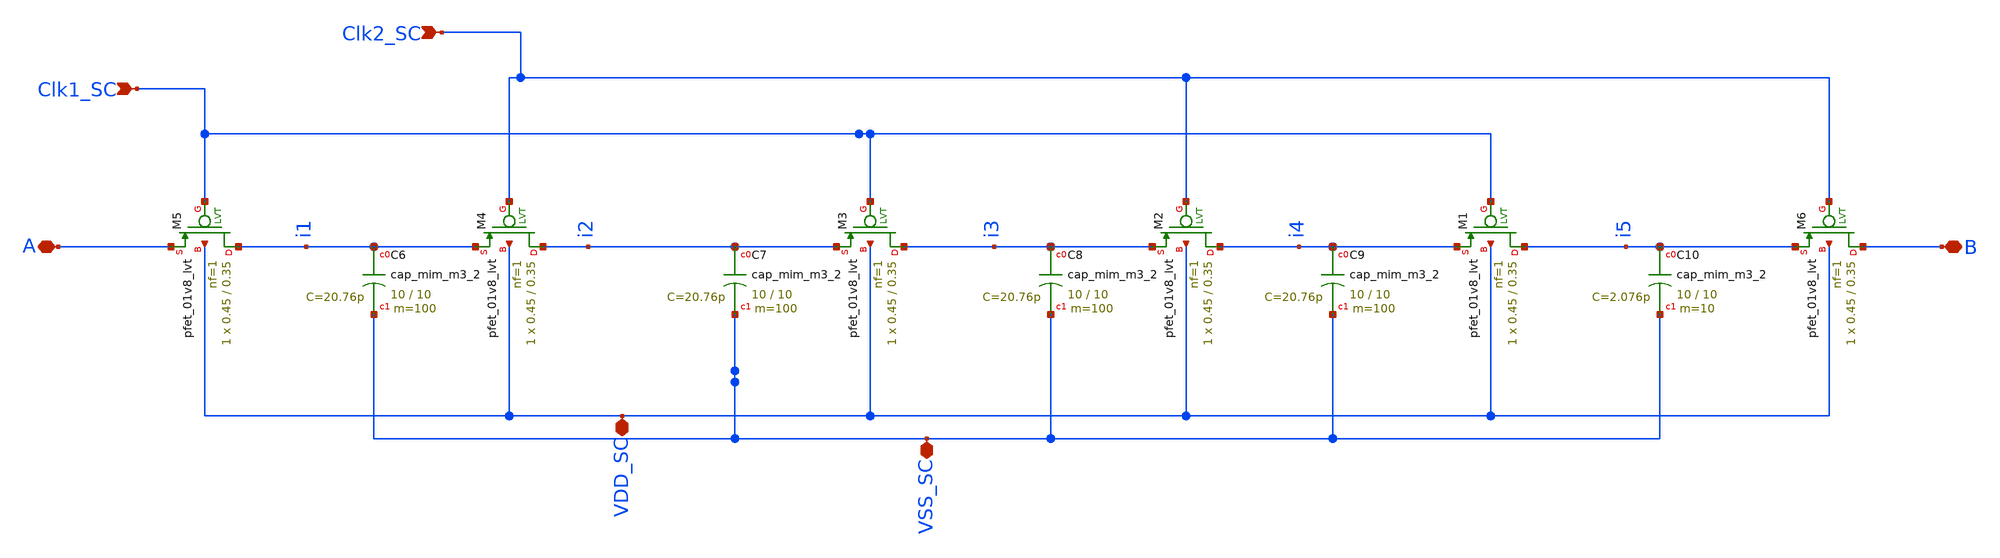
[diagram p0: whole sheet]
** sch_path: SC_bias.sch
**.subckt SC_bias A Clk1_SC Clk2_SC VSS_SC B VDD_SC
*.iopin A
*.ipin Clk1_SC
*.ipin Clk2_SC
*.iopin VSS_SC
*.iopin B
*.iopin VDD_SC
XM1 i5 Clk1_SC i4 VDD_SC sky130_fd_pr__pfet_01v8_lvt L=0.35 W=0.45 nf=1 ad='int((nf+1)/2) * W/nf * 0.29'
+ as='int((nf+2)/2) * W/nf * 0.29' pd='2*int((nf+1)/2) * (W/nf + 0.29)' ps='2*int((nf+2)/2) * (W/nf + 0.29)'
+ nrd='0.29 / W' nrs='0.29 / W' sa=0 sb=0 sd=0 mult=1 m=1
XM2 i4 Clk2_SC i3 VDD_SC sky130_fd_pr__pfet_01v8_lvt L=0.35 W=0.45 nf=1 ad='int((nf+1)/2) * W/nf * 0.29'
+ as='int((nf+2)/2) * W/nf * 0.29' pd='2*int((nf+1)/2) * (W/nf + 0.29)' ps='2*int((nf+2)/2) * (W/nf + 0.29)'
+ nrd='0.29 / W' nrs='0.29 / W' sa=0 sb=0 sd=0 mult=1 m=1
XM3 i3 Clk1_SC i2 VDD_SC sky130_fd_pr__pfet_01v8_lvt L=0.35 W=0.45 nf=1 ad='int((nf+1)/2) * W/nf * 0.29'
+ as='int((nf+2)/2) * W/nf * 0.29' pd='2*int((nf+1)/2) * (W/nf + 0.29)' ps='2*int((nf+2)/2) * (W/nf + 0.29)'
+ nrd='0.29 / W' nrs='0.29 / W' sa=0 sb=0 sd=0 mult=1 m=1
XM4 i2 Clk2_SC i1 VDD_SC sky130_fd_pr__pfet_01v8_lvt L=0.35 W=0.45 nf=1 ad='int((nf+1)/2) * W/nf * 0.29'
+ as='int((nf+2)/2) * W/nf * 0.29' pd='2*int((nf+1)/2) * (W/nf + 0.29)' ps='2*int((nf+2)/2) * (W/nf + 0.29)'
+ nrd='0.29 / W' nrs='0.29 / W' sa=0 sb=0 sd=0 mult=1 m=1
XM5 i1 Clk1_SC A VDD_SC sky130_fd_pr__pfet_01v8_lvt L=0.35 W=0.45 nf=1 ad='int((nf+1)/2) * W/nf * 0.29'
+ as='int((nf+2)/2) * W/nf * 0.29' pd='2*int((nf+1)/2) * (W/nf + 0.29)' ps='2*int((nf+2)/2) * (W/nf + 0.29)'
+ nrd='0.29 / W' nrs='0.29 / W' sa=0 sb=0 sd=0 mult=1 m=1
XM6 B Clk2_SC i5 VDD_SC sky130_fd_pr__pfet_01v8_lvt L=0.35 W=0.45 nf=1 ad='int((nf+1)/2) * W/nf * 0.29'
+ as='int((nf+2)/2) * W/nf * 0.29' pd='2*int((nf+1)/2) * (W/nf + 0.29)' ps='2*int((nf+2)/2) * (W/nf + 0.29)'
+ nrd='0.29 / W' nrs='0.29 / W' sa=0 sb=0 sd=0 mult=1 m=1
XC6 i1 VSS_SC sky130_fd_pr__cap_mim_m3_2 W=10 L=10 MF=100 m=100
XC7 i2 VSS_SC sky130_fd_pr__cap_mim_m3_2 W=10 L=10 MF=100 m=100
XC8 i3 VSS_SC sky130_fd_pr__cap_mim_m3_2 W=10 L=10 MF=100 m=100
XC9 i4 VSS_SC sky130_fd_pr__cap_mim_m3_2 W=10 L=10 MF=100 m=100
XC10 i5 VSS_SC sky130_fd_pr__cap_mim_m3_2 W=10 L=10 MF=10 m=10
**.ends
.end
